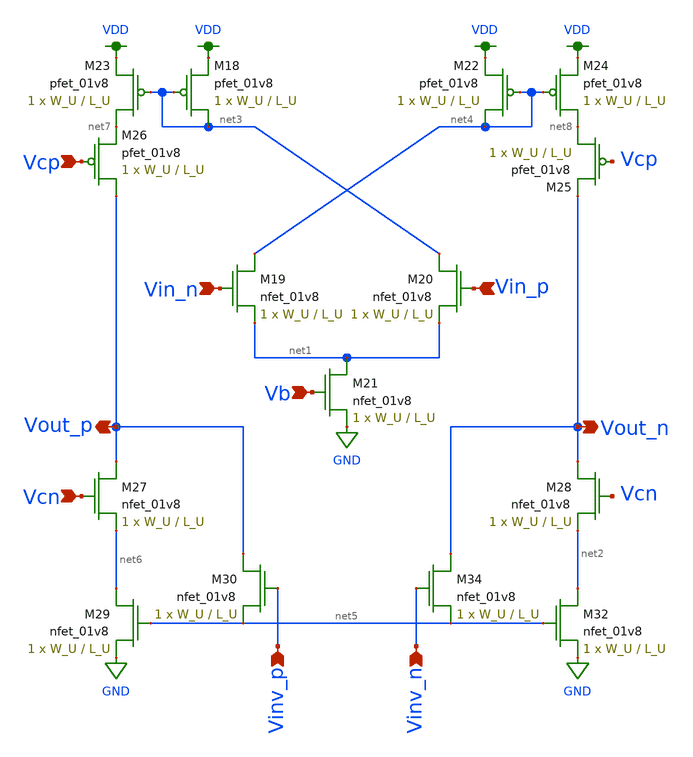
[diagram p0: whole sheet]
** sch_path: schematics/ota.sch
**.subckt ota Vin_n Vin_p Vout_n Vout_p Vcp Vb Vinv_p Vinv_n Vcn
*.ipin Vin_n
*.ipin Vin_p
*.opin Vout_n
*.opin Vout_p
*.ipin Vcp
*.ipin Vb
*.ipin Vinv_p
*.ipin Vinv_n
*.ipin Vcn
XM18 net3 net3 VDD VDD sky130_fd_pr__pfet_01v8 L=L_U W=W_U nf=1 ad='int((nf+1)/2) * W/nf * 0.29' as='int((nf+2)/2) * W/nf * 0.29'
+ pd='2*int((nf+1)/2) * (W/nf + 0.29)' ps='2*int((nf+2)/2) * (W/nf + 0.29)' nrd='0.29 / W' nrs='0.29 / W'
+ sa=0 sb=0 sd=0 mult=1 m=1
XM19 net4 Vin_n net1 GND sky130_fd_pr__nfet_01v8 L=L_U W=W_U nf=1 ad='int((nf+1)/2) * W/nf * 0.29' as='int((nf+2)/2) * W/nf * 0.29'
+ pd='2*int((nf+1)/2) * (W/nf + 0.29)' ps='2*int((nf+2)/2) * (W/nf + 0.29)' nrd='0.29 / W' nrs='0.29 / W'
+ sa=0 sb=0 sd=0 mult=1 m=1
XM20 net3 Vin_p net1 GND sky130_fd_pr__nfet_01v8 L=L_U W=W_U nf=1 ad='int((nf+1)/2) * W/nf * 0.29' as='int((nf+2)/2) * W/nf * 0.29'
+ pd='2*int((nf+1)/2) * (W/nf + 0.29)' ps='2*int((nf+2)/2) * (W/nf + 0.29)' nrd='0.29 / W' nrs='0.29 / W'
+ sa=0 sb=0 sd=0 mult=1 m=1
XM21 net1 Vb GND GND sky130_fd_pr__nfet_01v8 L=L_U W=W_U nf=1 ad='int((nf+1)/2) * W/nf * 0.29' as='int((nf+2)/2) * W/nf * 0.29'
+ pd='2*int((nf+1)/2) * (W/nf + 0.29)' ps='2*int((nf+2)/2) * (W/nf + 0.29)' nrd='0.29 / W' nrs='0.29 / W'
+ sa=0 sb=0 sd=0 mult=1 m=1
XM22 net4 net4 VDD VDD sky130_fd_pr__pfet_01v8 L=L_U W=W_U nf=1 ad='int((nf+1)/2) * W/nf * 0.29' as='int((nf+2)/2) * W/nf * 0.29'
+ pd='2*int((nf+1)/2) * (W/nf + 0.29)' ps='2*int((nf+2)/2) * (W/nf + 0.29)' nrd='0.29 / W' nrs='0.29 / W'
+ sa=0 sb=0 sd=0 mult=1 m=1
XM23 net7 net3 VDD VDD sky130_fd_pr__pfet_01v8 L=L_U W=W_U nf=1 ad='int((nf+1)/2) * W/nf * 0.29' as='int((nf+2)/2) * W/nf * 0.29'
+ pd='2*int((nf+1)/2) * (W/nf + 0.29)' ps='2*int((nf+2)/2) * (W/nf + 0.29)' nrd='0.29 / W' nrs='0.29 / W'
+ sa=0 sb=0 sd=0 mult=1 m=1
XM24 net8 net4 VDD VDD sky130_fd_pr__pfet_01v8 L=L_U W=W_U nf=1 ad='int((nf+1)/2) * W/nf * 0.29' as='int((nf+2)/2) * W/nf * 0.29'
+ pd='2*int((nf+1)/2) * (W/nf + 0.29)' ps='2*int((nf+2)/2) * (W/nf + 0.29)' nrd='0.29 / W' nrs='0.29 / W'
+ sa=0 sb=0 sd=0 mult=1 m=1
XM25 net8 Vcp Vout_n VDD sky130_fd_pr__pfet_01v8 L=L_U W=W_U nf=1 ad='int((nf+1)/2) * W/nf * 0.29' as='int((nf+2)/2) * W/nf * 0.29'
+ pd='2*int((nf+1)/2) * (W/nf + 0.29)' ps='2*int((nf+2)/2) * (W/nf + 0.29)' nrd='0.29 / W' nrs='0.29 / W'
+ sa=0 sb=0 sd=0 mult=1 m=1
XM26 Vout_p Vcp net7 VDD sky130_fd_pr__pfet_01v8 L=L_U W=W_U nf=1 ad='int((nf+1)/2) * W/nf * 0.29' as='int((nf+2)/2) * W/nf * 0.29'
+ pd='2*int((nf+1)/2) * (W/nf + 0.29)' ps='2*int((nf+2)/2) * (W/nf + 0.29)' nrd='0.29 / W' nrs='0.29 / W'
+ sa=0 sb=0 sd=0 mult=1 m=1
XM27 Vout_p Vcn net6 GND sky130_fd_pr__nfet_01v8 L=L_U W=W_U nf=1 ad='int((nf+1)/2) * W/nf * 0.29' as='int((nf+2)/2) * W/nf * 0.29'
+ pd='2*int((nf+1)/2) * (W/nf + 0.29)' ps='2*int((nf+2)/2) * (W/nf + 0.29)' nrd='0.29 / W' nrs='0.29 / W'
+ sa=0 sb=0 sd=0 mult=1 m=1
XM28 Vout_n Vcn net2 GND sky130_fd_pr__nfet_01v8 L=L_U W=W_U nf=1 ad='int((nf+1)/2) * W/nf * 0.29' as='int((nf+2)/2) * W/nf * 0.29'
+ pd='2*int((nf+1)/2) * (W/nf + 0.29)' ps='2*int((nf+2)/2) * (W/nf + 0.29)' nrd='0.29 / W' nrs='0.29 / W'
+ sa=0 sb=0 sd=0 mult=1 m=1
XM29 net6 net5 GND GND sky130_fd_pr__nfet_01v8 L=L_U W=W_U nf=1 ad='int((nf+1)/2) * W/nf * 0.29' as='int((nf+2)/2) * W/nf * 0.29'
+ pd='2*int((nf+1)/2) * (W/nf + 0.29)' ps='2*int((nf+2)/2) * (W/nf + 0.29)' nrd='0.29 / W' nrs='0.29 / W'
+ sa=0 sb=0 sd=0 mult=1 m=1
XM30 Vout_p Vinv_p net5 GND sky130_fd_pr__nfet_01v8 L=L_U W=W_U nf=1 ad='int((nf+1)/2) * W/nf * 0.29'
+ as='int((nf+2)/2) * W/nf * 0.29' pd='2*int((nf+1)/2) * (W/nf + 0.29)' ps='2*int((nf+2)/2) * (W/nf + 0.29)'
+ nrd='0.29 / W' nrs='0.29 / W' sa=0 sb=0 sd=0 mult=1 m=1
XM32 net2 net5 GND GND sky130_fd_pr__nfet_01v8 L=L_U W=W_U nf=1 ad='int((nf+1)/2) * W/nf * 0.29' as='int((nf+2)/2) * W/nf * 0.29'
+ pd='2*int((nf+1)/2) * (W/nf + 0.29)' ps='2*int((nf+2)/2) * (W/nf + 0.29)' nrd='0.29 / W' nrs='0.29 / W'
+ sa=0 sb=0 sd=0 mult=1 m=1
XM34 Vout_n Vinv_n net5 GND sky130_fd_pr__nfet_01v8 L=L_U W=W_U nf=1 ad='int((nf+1)/2) * W/nf * 0.29'
+ as='int((nf+2)/2) * W/nf * 0.29' pd='2*int((nf+1)/2) * (W/nf + 0.29)' ps='2*int((nf+2)/2) * (W/nf + 0.29)'
+ nrd='0.29 / W' nrs='0.29 / W' sa=0 sb=0 sd=0 mult=1 m=1
**.ends
.GLOBAL VDD
.GLOBAL GND
.end
